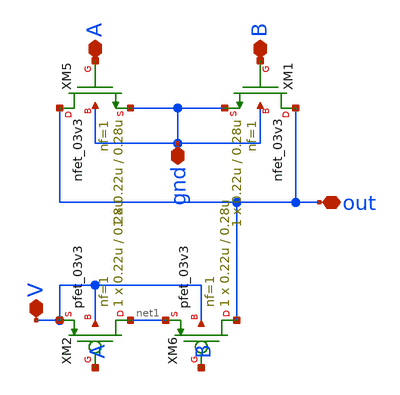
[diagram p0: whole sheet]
** sch_path: xschem/nor_gate.sch
**.subckt nor_gate A out gnd V B
*.iopin A
*.iopin out
*.iopin gnd
*.iopin V
*.iopin B
XM5 out A gnd gnd nfet_03v3 L=0.28u W=0.22u nf=1 ad='int((nf+1)/2) * W/nf * 0.18u' as='int((nf+2)/2) * W/nf * 0.18u'
+ pd='2*int((nf+1)/2) * (W/nf + 0.18u)' ps='2*int((nf+2)/2) * (W/nf + 0.18u)' nrd='0.18u / W' nrs='0.18u / W'
+ sa=0 sb=0 sd=0 m=1
XM6 out B net1 V pfet_03v3 L=0.28u W=0.22u nf=1 ad='int((nf+1)/2) * W/nf * 0.18u' as='int((nf+2)/2) * W/nf * 0.18u'
+ pd='2*int((nf+1)/2) * (W/nf + 0.18u)' ps='2*int((nf+2)/2) * (W/nf + 0.18u)' nrd='0.18u / W' nrs='0.18u / W'
+ sa=0 sb=0 sd=0 m=1
XM1 out B gnd gnd nfet_03v3 L=0.28u W=0.22u nf=1 ad='int((nf+1)/2) * W/nf * 0.18u' as='int((nf+2)/2) * W/nf * 0.18u'
+ pd='2*int((nf+1)/2) * (W/nf + 0.18u)' ps='2*int((nf+2)/2) * (W/nf + 0.18u)' nrd='0.18u / W' nrs='0.18u / W'
+ sa=0 sb=0 sd=0 m=1
XM2 net1 A V V pfet_03v3 L=0.28u W=0.22u nf=1 ad='int((nf+1)/2) * W/nf * 0.18u' as='int((nf+2)/2) * W/nf * 0.18u'
+ pd='2*int((nf+1)/2) * (W/nf + 0.18u)' ps='2*int((nf+2)/2) * (W/nf + 0.18u)' nrd='0.18u / W' nrs='0.18u / W'
+ sa=0 sb=0 sd=0 m=1
**.ends
.end
